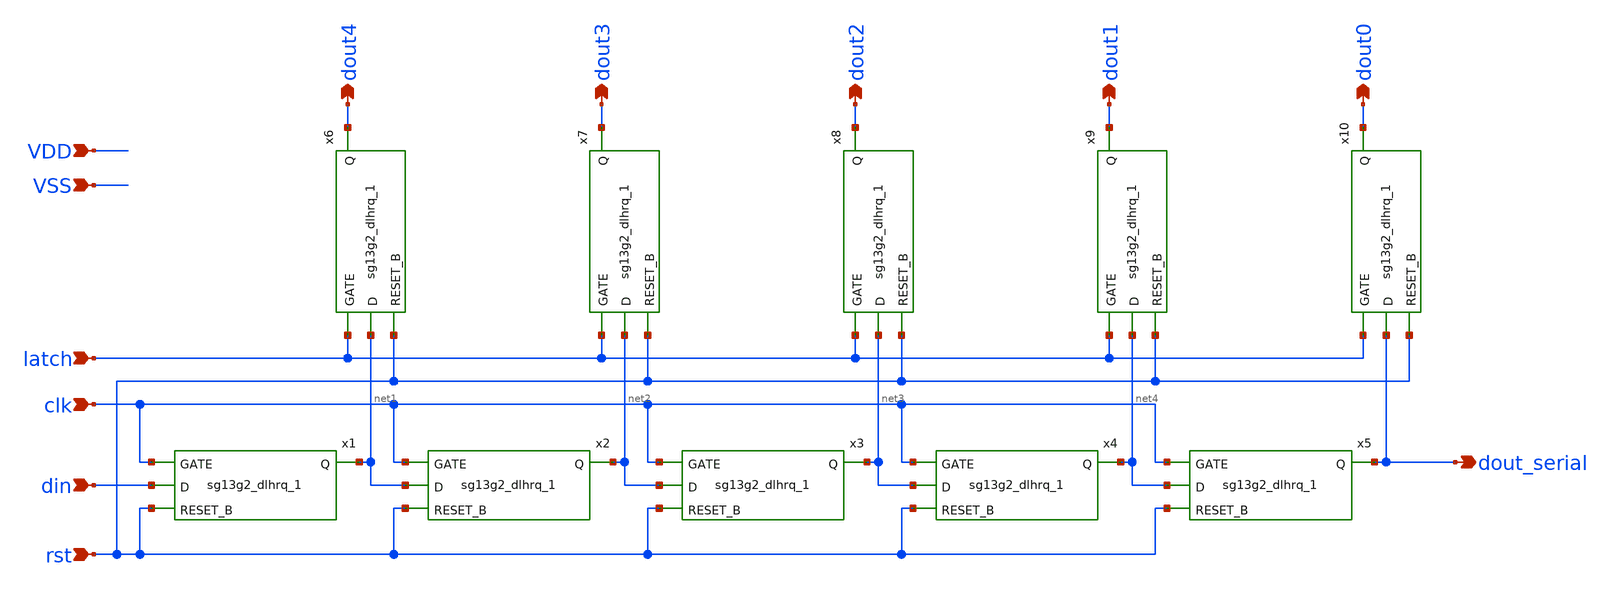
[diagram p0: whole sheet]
** sch_path: xschem/digital/shift_reg_raro.sch
**.subckt shift_reg_raro din rst clk dout3 dout0 dout1 dout2 dout4 latch VDD VSS dout_serial
*.ipin din
*.ipin rst
*.ipin clk
*.opin dout3
*.opin dout0
*.opin dout1
*.opin dout2
*.opin dout4
*.ipin latch
*.ipin VDD
*.ipin VSS
*.opin dout_serial
x1 din rst VGND VNB VPB VPWR net1 sg13g2_dlhrq_1
x2 net1 rst VGND VNB VPB VPWR net2 sg13g2_dlhrq_1
x3 net2 rst VGND VNB VPB VPWR net3 sg13g2_dlhrq_1
x4 net3 rst VGND VNB VPB VPWR net4 sg13g2_dlhrq_1
x5 net4 rst VGND VNB VPB VPWR dout_serial sg13g2_dlhrq_1
x6 net1 rst VGND VNB VPB VPWR dout4 sg13g2_dlhrq_1
x7 net2 rst VGND VNB VPB VPWR dout3 sg13g2_dlhrq_1
x8 net3 rst VGND VNB VPB VPWR dout2 sg13g2_dlhrq_1
x9 net4 rst VGND VNB VPB VPWR dout1 sg13g2_dlhrq_1
x10 dout_serial rst VGND VNB VPB VPWR dout0 sg13g2_dlhrq_1
**.ends
.end
